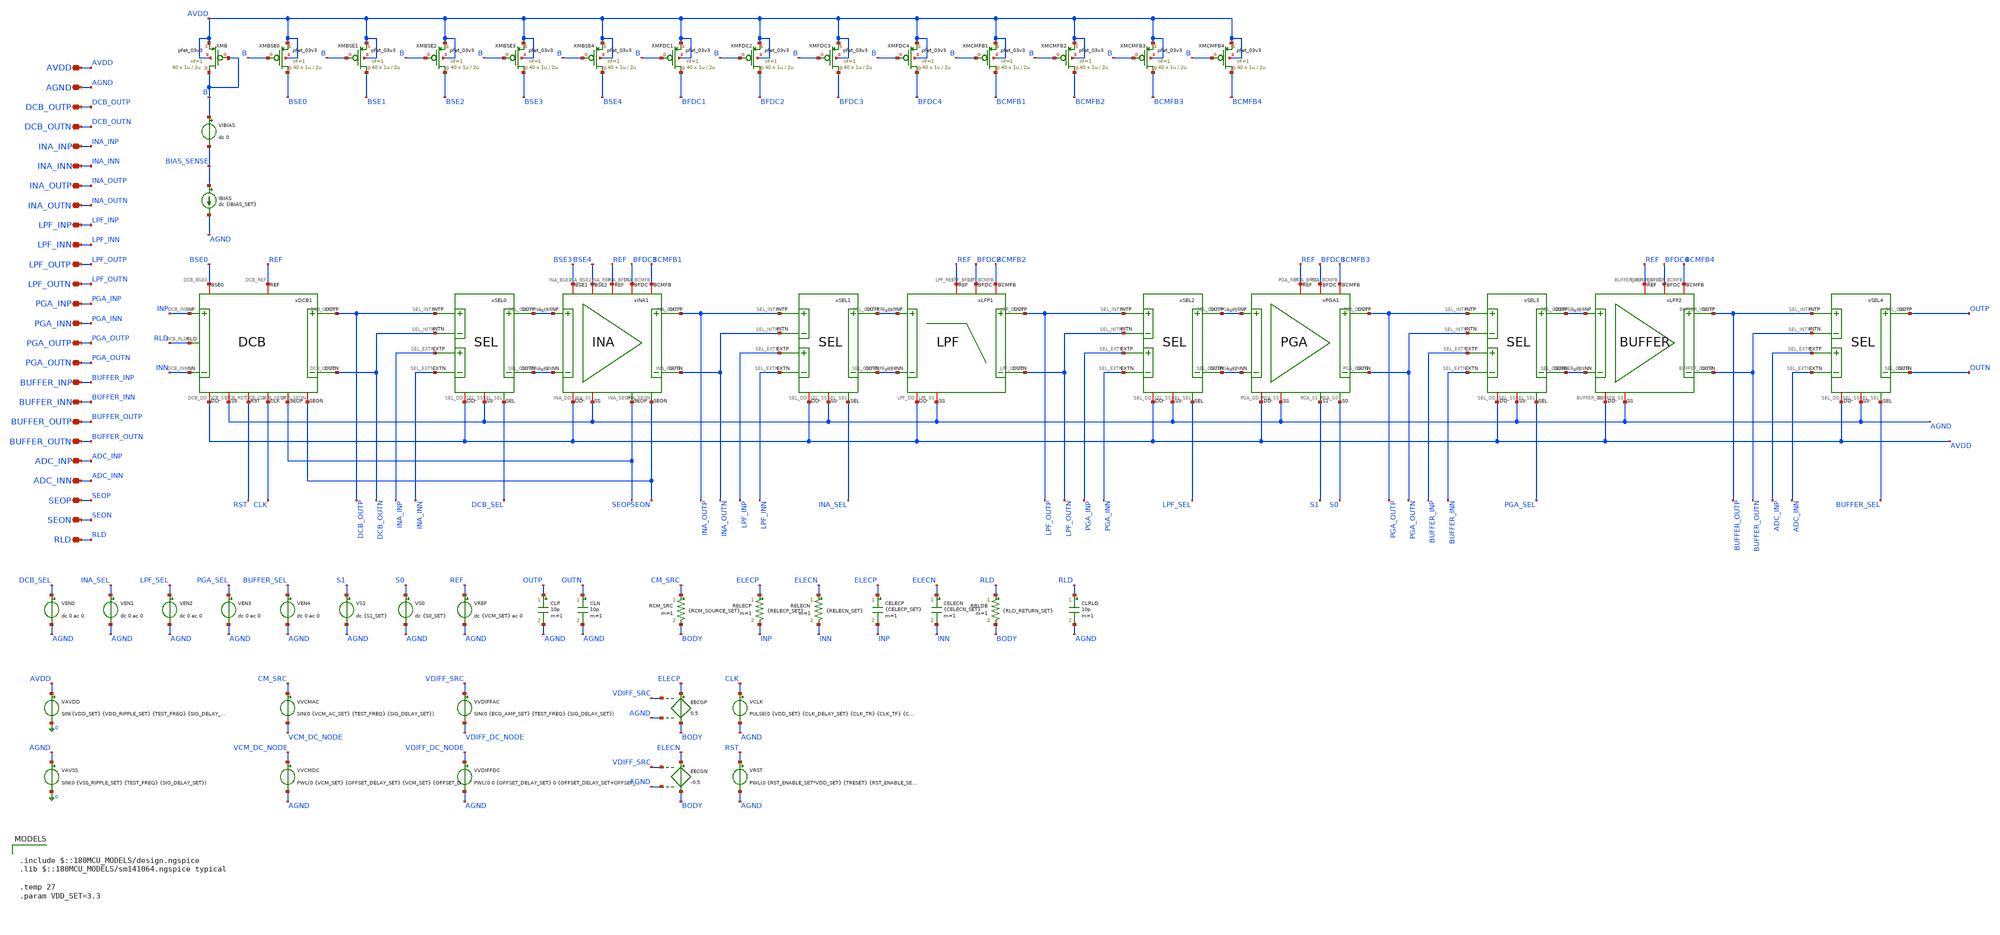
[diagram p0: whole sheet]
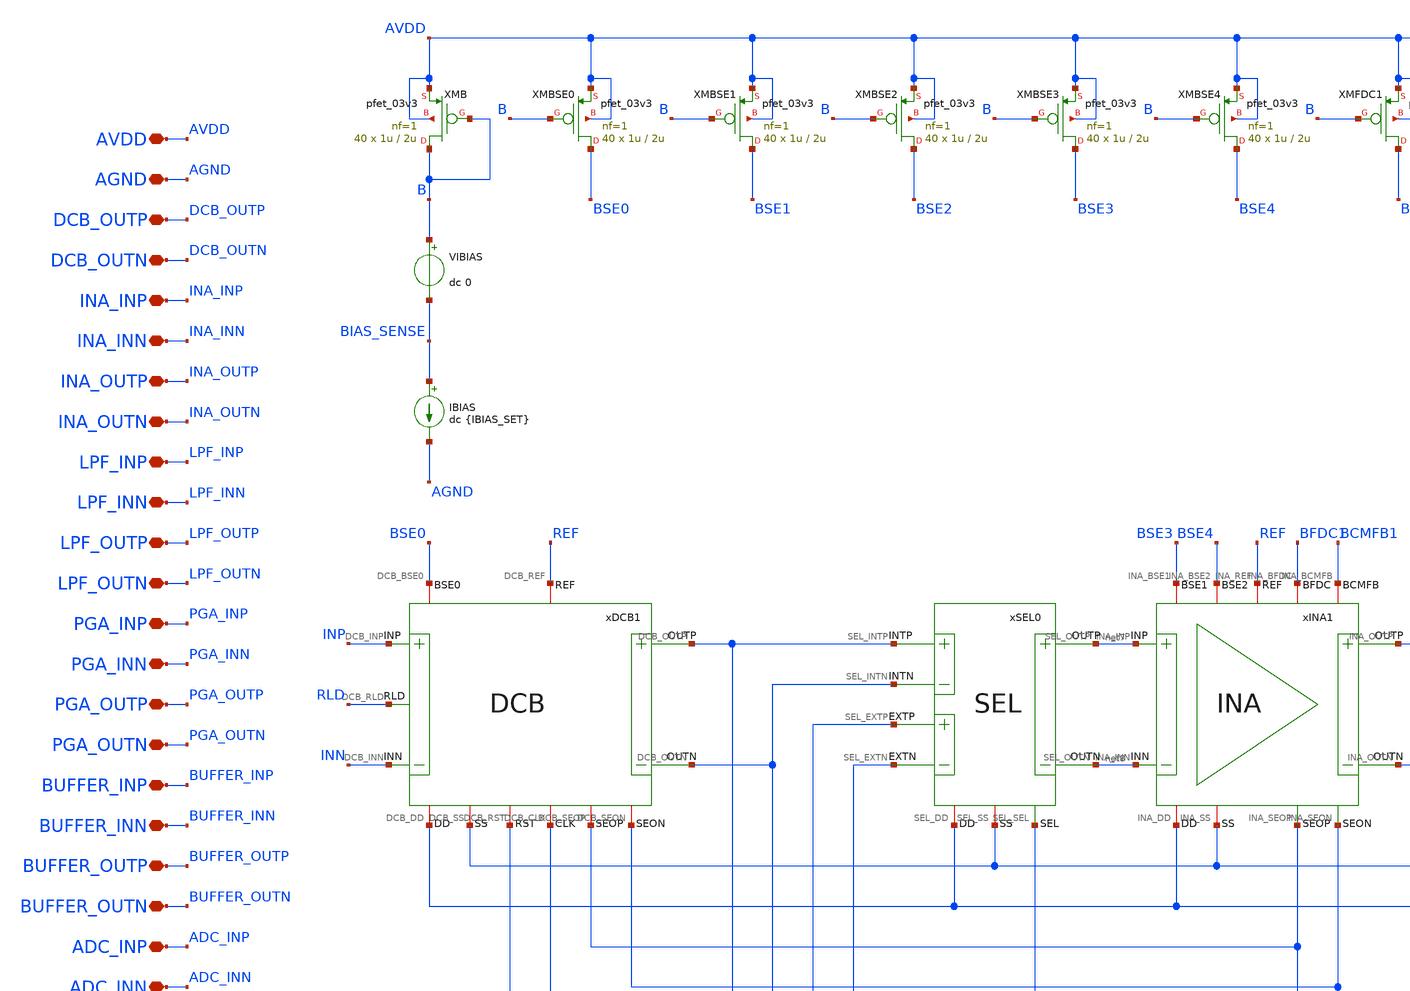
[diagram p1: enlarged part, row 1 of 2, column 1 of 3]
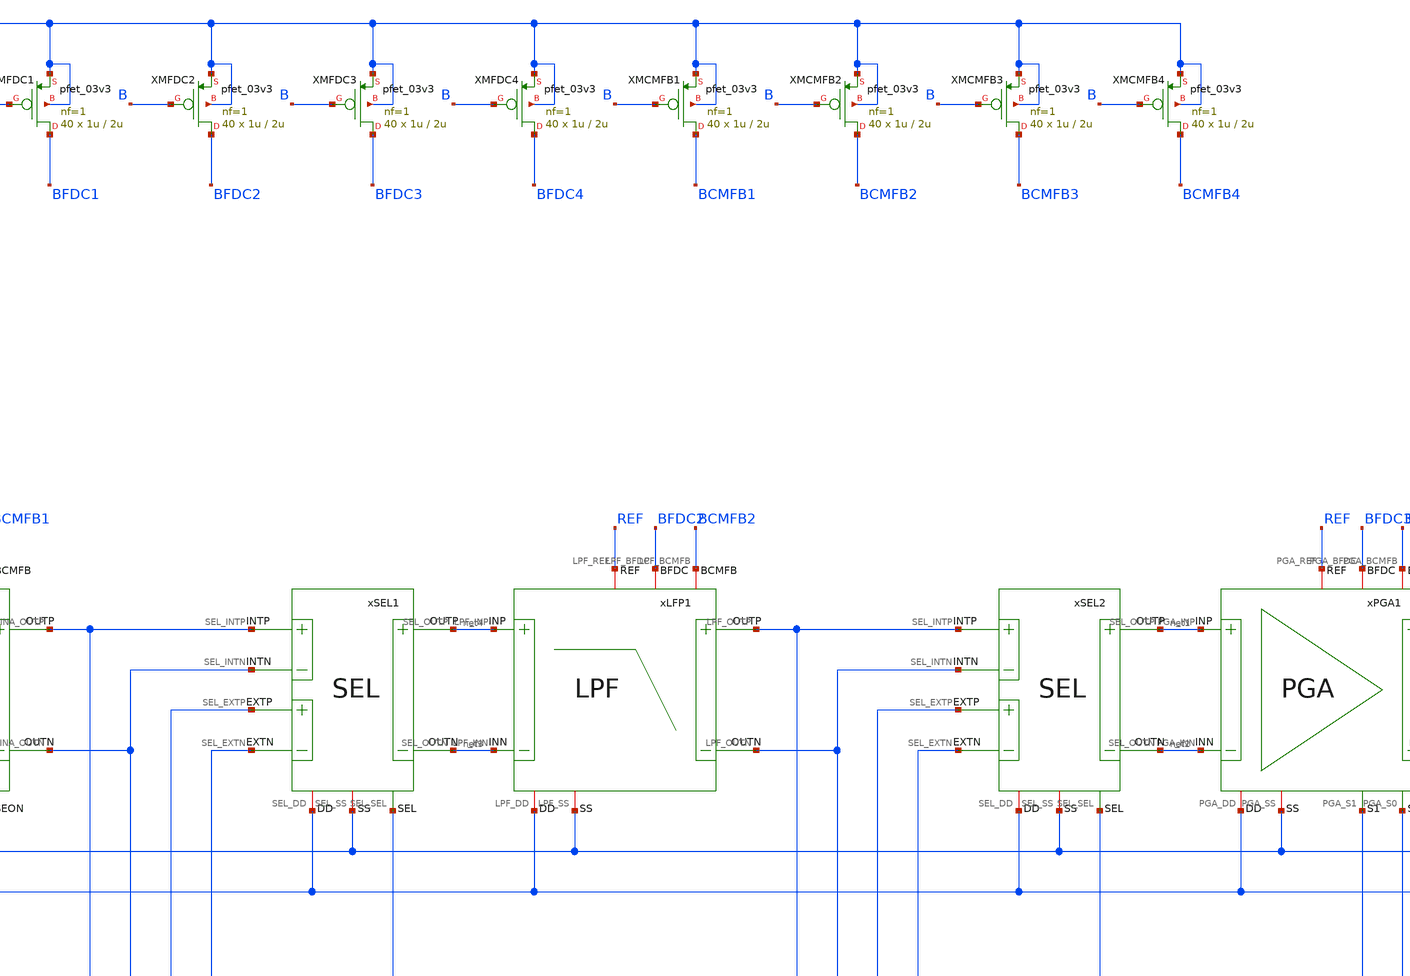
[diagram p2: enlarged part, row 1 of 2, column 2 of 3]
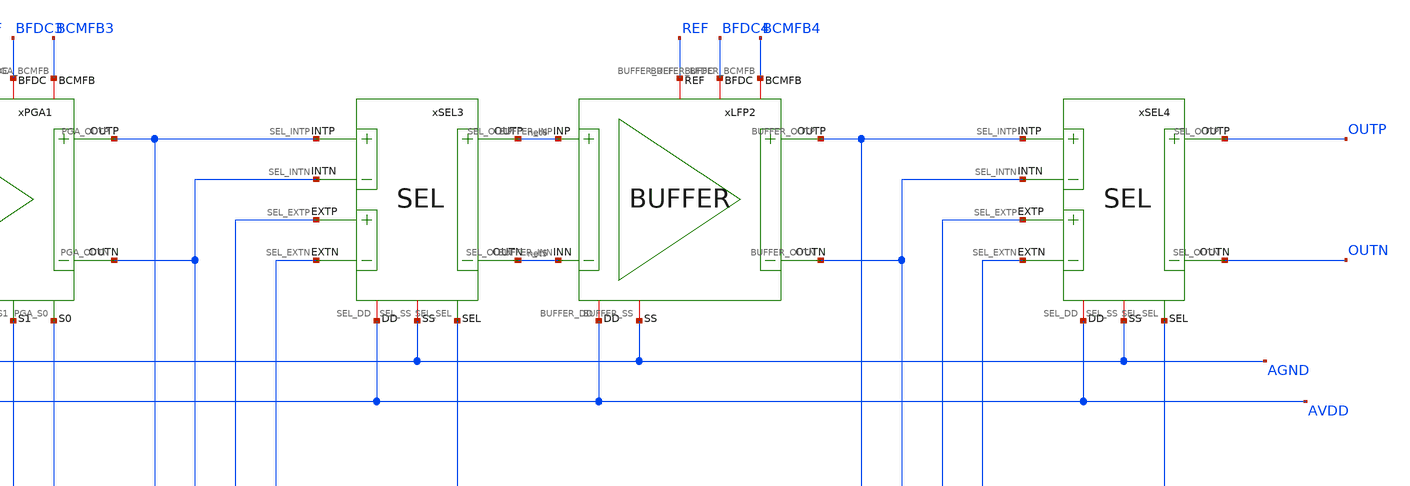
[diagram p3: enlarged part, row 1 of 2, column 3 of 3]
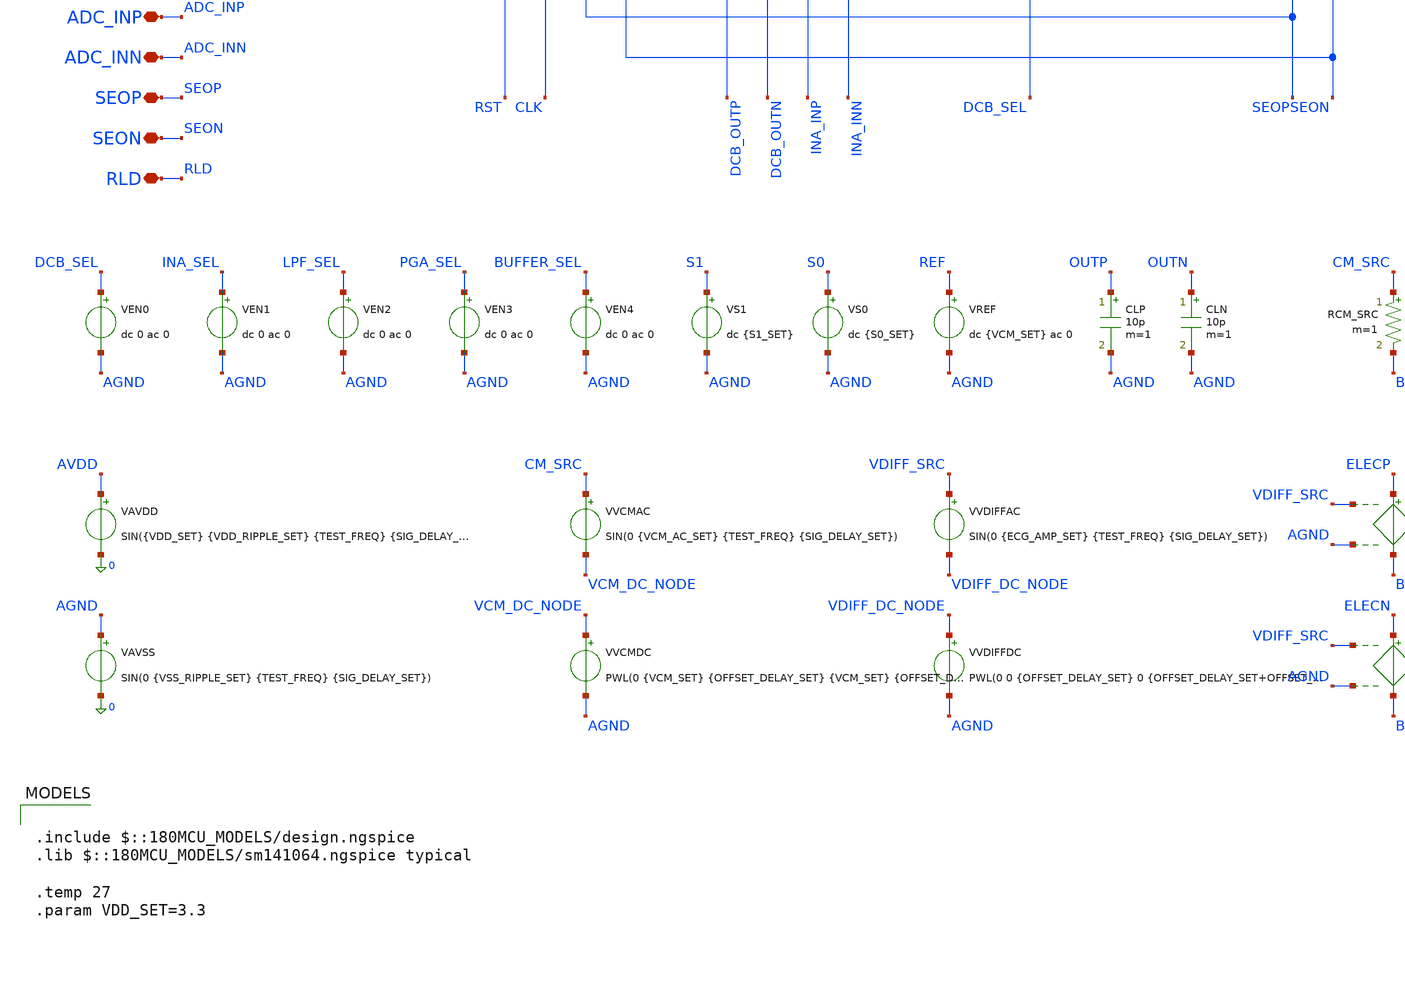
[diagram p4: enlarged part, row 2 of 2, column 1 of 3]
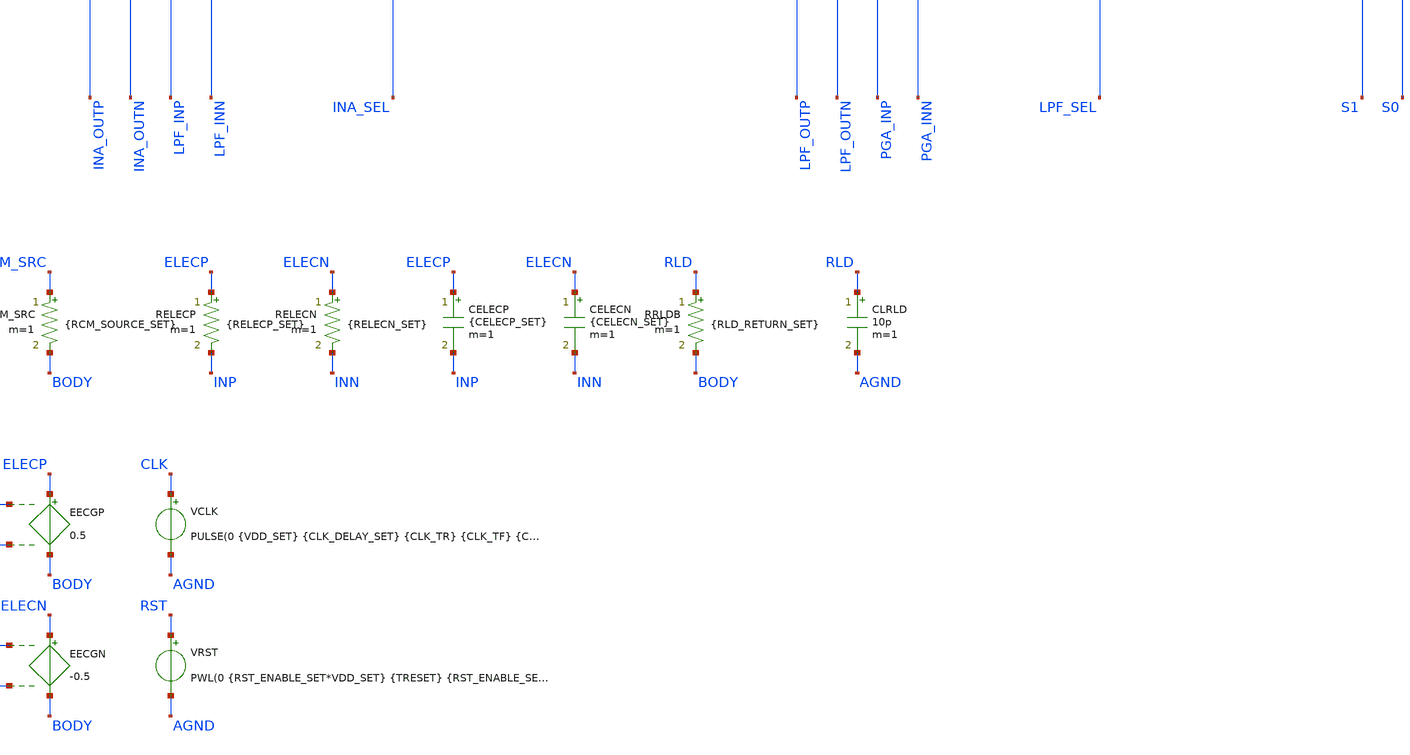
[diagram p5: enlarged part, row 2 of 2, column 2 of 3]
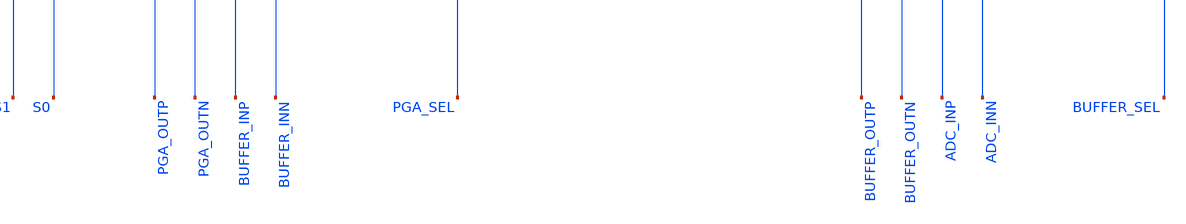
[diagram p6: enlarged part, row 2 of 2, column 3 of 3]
** sch_path: Design_Files/IC Design/Testbench/PATH/TRAN/PATH_TB_TRAN.sch
**.subckt PATH_TB_TRAN DCB_OUTP DCB_OUTN INA_INP INA_INN INA_OUTP INA_OUTN LPF_INP LPF_INN LPF_OUTP
*+ LPF_OUTN PGA_INP PGA_INN PGA_OUTP PGA_OUTN BUFFER_INP BUFFER_INN BUFFER_OUTP BUFFER_OUTN ADC_INP ADC_INN
*+ AVDD AGND SEOP SEON RLD
*.iopin DCB_OUTP
*.iopin DCB_OUTN
*.iopin INA_INP
*.iopin INA_INN
*.iopin INA_OUTP
*.iopin INA_OUTN
*.iopin LPF_INP
*.iopin LPF_INN
*.iopin LPF_OUTP
*.iopin LPF_OUTN
*.iopin PGA_INP
*.iopin PGA_INN
*.iopin PGA_OUTP
*.iopin PGA_OUTN
*.iopin BUFFER_INP
*.iopin BUFFER_INN
*.iopin BUFFER_OUTP
*.iopin BUFFER_OUTN
*.iopin ADC_INP
*.iopin ADC_INN
*.iopin AVDD
*.iopin AGND
*.iopin SEOP
*.iopin SEON
*.iopin RLD
VAVDD AVDD 0 SIN({VDD_SET} {VDD_RIPPLE_SET} {TEST_FREQ} {SIG_DELAY_SET})
.save i(vavdd)
VAVSS AGND 0 SIN(0 {VSS_RIPPLE_SET} {TEST_FREQ} {SIG_DELAY_SET})
.save i(vavss)
CLP OUTP AGND 10p m=1
CLN OUTN AGND 10p m=1
VIBIAS B BIAS_SENSE dc 0
.save i(vibias)
IBIAS BIAS_SENSE AGND dc {IBIAS_SET}
VREF REF AGND dc {VCM_SET} ac 0
xLFP1 AVDD AGND net4 net3 LPF_OUTN BFDC2 LPF_OUTP BCMFB2 REF LPF
xPGA1 AVDD AGND net1 net2 PGA_OUTN BFDC3 PGA_OUTP BCMFB3 REF S1 S0 PGA
xSEL1 AVDD AGND INA_OUTP INA_OUTN net3 net4 LPF_INP LPF_INN INA_SEL SEL
xINA1 AVDD AGND net7 net8 INA_OUTN BFDC1 INA_OUTP BCMFB1 REF SEON SEOP BSE3 BSE4 INA
xSEL2 AVDD AGND LPF_OUTP LPF_OUTN net2 net1 PGA_INP PGA_INN LPF_SEL SEL
xSEL3 AVDD AGND PGA_OUTP PGA_OUTN net5 net6 BUFFER_INP BUFFER_INN PGA_SEL SEL
xSEL4 AVDD AGND BUFFER_OUTP BUFFER_OUTN OUTN OUTP ADC_INP ADC_INN BUFFER_SEL SEL
xLFP2 AVDD AGND net6 net5 BUFFER_OUTN BFDC4 BUFFER_OUTP BCMFB4 REF BUFFER
VEN1 INA_SEL AGND dc 0 ac 0
.save i(ven1)
VS0 S0 AGND dc {S0_SET}
VS1 S1 AGND dc {S1_SET}
xSEL0 AVDD AGND DCB_OUTP DCB_OUTN net8 net7 INA_INP INA_INN DCB_SEL SEL
xDCB1 AVDD AGND INP INN DCB_OUTP DCB_OUTN RST CLK SEOP SEON REF BSE0 RLD DCB
VEN2 LPF_SEL AGND dc 0 ac 0
.save i(ven2)
VEN3 PGA_SEL AGND dc 0 ac 0
.save i(ven3)
VEN4 BUFFER_SEL AGND dc 0 ac 0
.save i(ven4)
VEN0 DCB_SEL AGND dc 0 ac 0
.save i(ven0)
VRST RST AGND PWL(0 {RST_ENABLE_SET*VDD_SET} {TRESET} {RST_ENABLE_SET*VDD_SET} {TRESET_END} 0 {RST_PULSE_ON_SET}
+ 0 {RST_PULSE_ON_END_SET} {RST_PULSE_ENABLE_SET*VDD_SET} {RST_PULSE_OFF_SET} {RST_PULSE_ENABLE_SET*VDD_SET}
+ {RST_PULSE_OFF_END_SET} 0)
VCLK CLK AGND PULSE(0 {VDD_SET} {CLK_DELAY_SET} {CLK_TR} {CLK_TF} {CLK_PW} {1/CLK_FREQ})
.save i(vclk)
CLRLD RLD AGND 10p m=1
RCM_SRC CM_SRC BODY {RCM_SOURCE_SET} m=1
RELECP ELECP INP {RELECP_SET} m=1
RELECN ELECN INN {RELECN_SET} m=1
CELECP ELECP INP {CELECP_SET} m=1
CELECN ELECN INN {CELECN_SET} m=1
RRLDB RLD BODY {RLD_RETURN_SET} m=1
VVCMAC CM_SRC VCM_DC_NODE SIN(0 {VCM_AC_SET} {TEST_FREQ} {SIG_DELAY_SET})
VVCMDC VCM_DC_NODE AGND PWL(0 {VCM_SET} {OFFSET_DELAY_SET} {VCM_SET} {OFFSET_DELAY_SET+OFFSET_RISE_SET}
+ {VCM_SET+VCM_DC_SET})
VVDIFFAC VDIFF_SRC VDIFF_DC_NODE SIN(0 {ECG_AMP_SET} {TEST_FREQ} {SIG_DELAY_SET})
VVDIFFDC VDIFF_DC_NODE AGND PWL(0 0 {OFFSET_DELAY_SET} 0 {OFFSET_DELAY_SET+OFFSET_RISE_SET} {VDIFF_DC_SET})
EECGP ELECP BODY VDIFF_SRC AGND 0.5
EECGN ELECN BODY VDIFF_SRC AGND -0.5
XMB B B AVDD AVDD pfet_03v3 L=2u W=1u nf=1 ad='int((nf+1)/2) * W/nf * 0.18u' as='int((nf+2)/2) * W/nf * 0.18u'
+ pd='2*int((nf+1)/2) * (W/nf + 0.18u)' ps='2*int((nf+2)/2) * (W/nf + 0.18u)' nrd='0.18u / W' nrs='0.18u / W'
+ sa=0 sb=0 sd=0 m=40
XMBSE3 BSE3 B AVDD AVDD pfet_03v3 L=2u W=1u nf=1 ad='int((nf+1)/2) * W/nf * 0.18u' as='int((nf+2)/2) * W/nf * 0.18u'
+ pd='2*int((nf+1)/2) * (W/nf + 0.18u)' ps='2*int((nf+2)/2) * (W/nf + 0.18u)' nrd='0.18u / W' nrs='0.18u / W'
+ sa=0 sb=0 sd=0 m=40
XMBSE4 BSE4 B AVDD AVDD pfet_03v3 L=2u W=1u nf=1 ad='int((nf+1)/2) * W/nf * 0.18u' as='int((nf+2)/2) * W/nf * 0.18u'
+ pd='2*int((nf+1)/2) * (W/nf + 0.18u)' ps='2*int((nf+2)/2) * (W/nf + 0.18u)' nrd='0.18u / W' nrs='0.18u / W'
+ sa=0 sb=0 sd=0 m=40
XMFDC1 BFDC1 B AVDD AVDD pfet_03v3 L=2u W=1u nf=1 ad='int((nf+1)/2) * W/nf * 0.18u' as='int((nf+2)/2) * W/nf * 0.18u'
+ pd='2*int((nf+1)/2) * (W/nf + 0.18u)' ps='2*int((nf+2)/2) * (W/nf + 0.18u)' nrd='0.18u / W' nrs='0.18u / W'
+ sa=0 sb=0 sd=0 m=40
XMFDC2 BFDC2 B AVDD AVDD pfet_03v3 L=2u W=1u nf=1 ad='int((nf+1)/2) * W/nf * 0.18u' as='int((nf+2)/2) * W/nf * 0.18u'
+ pd='2*int((nf+1)/2) * (W/nf + 0.18u)' ps='2*int((nf+2)/2) * (W/nf + 0.18u)' nrd='0.18u / W' nrs='0.18u / W'
+ sa=0 sb=0 sd=0 m=40
XMFDC3 BFDC3 B AVDD AVDD pfet_03v3 L=2u W=1u nf=1 ad='int((nf+1)/2) * W/nf * 0.18u' as='int((nf+2)/2) * W/nf * 0.18u'
+ pd='2*int((nf+1)/2) * (W/nf + 0.18u)' ps='2*int((nf+2)/2) * (W/nf + 0.18u)' nrd='0.18u / W' nrs='0.18u / W'
+ sa=0 sb=0 sd=0 m=40
XMFDC4 BFDC4 B AVDD AVDD pfet_03v3 L=2u W=1u nf=1 ad='int((nf+1)/2) * W/nf * 0.18u' as='int((nf+2)/2) * W/nf * 0.18u'
+ pd='2*int((nf+1)/2) * (W/nf + 0.18u)' ps='2*int((nf+2)/2) * (W/nf + 0.18u)' nrd='0.18u / W' nrs='0.18u / W'
+ sa=0 sb=0 sd=0 m=40
XMCMFB1 BCMFB1 B AVDD AVDD pfet_03v3 L=2u W=1u nf=1 ad='int((nf+1)/2) * W/nf * 0.18u' as='int((nf+2)/2) * W/nf * 0.18u'
+ pd='2*int((nf+1)/2) * (W/nf + 0.18u)' ps='2*int((nf+2)/2) * (W/nf + 0.18u)' nrd='0.18u / W' nrs='0.18u / W'
+ sa=0 sb=0 sd=0 m=40
XMCMFB2 BCMFB2 B AVDD AVDD pfet_03v3 L=2u W=1u nf=1 ad='int((nf+1)/2) * W/nf * 0.18u' as='int((nf+2)/2) * W/nf * 0.18u'
+ pd='2*int((nf+1)/2) * (W/nf + 0.18u)' ps='2*int((nf+2)/2) * (W/nf + 0.18u)' nrd='0.18u / W' nrs='0.18u / W'
+ sa=0 sb=0 sd=0 m=40
XMCMFB3 BCMFB3 B AVDD AVDD pfet_03v3 L=2u W=1u nf=1 ad='int((nf+1)/2) * W/nf * 0.18u' as='int((nf+2)/2) * W/nf * 0.18u'
+ pd='2*int((nf+1)/2) * (W/nf + 0.18u)' ps='2*int((nf+2)/2) * (W/nf + 0.18u)' nrd='0.18u / W' nrs='0.18u / W'
+ sa=0 sb=0 sd=0 m=40
XMCMFB4 BCMFB4 B AVDD AVDD pfet_03v3 L=2u W=1u nf=1 ad='int((nf+1)/2) * W/nf * 0.18u' as='int((nf+2)/2) * W/nf * 0.18u'
+ pd='2*int((nf+1)/2) * (W/nf + 0.18u)' ps='2*int((nf+2)/2) * (W/nf + 0.18u)' nrd='0.18u / W' nrs='0.18u / W'
+ sa=0 sb=0 sd=0 m=40
XMBSE1 BSE1 B AVDD AVDD pfet_03v3 L=2u W=1u nf=1 ad='int((nf+1)/2) * W/nf * 0.18u' as='int((nf+2)/2) * W/nf * 0.18u'
+ pd='2*int((nf+1)/2) * (W/nf + 0.18u)' ps='2*int((nf+2)/2) * (W/nf + 0.18u)' nrd='0.18u / W' nrs='0.18u / W'
+ sa=0 sb=0 sd=0 m=40
XMBSE2 BSE2 B AVDD AVDD pfet_03v3 L=2u W=1u nf=1 ad='int((nf+1)/2) * W/nf * 0.18u' as='int((nf+2)/2) * W/nf * 0.18u'
+ pd='2*int((nf+1)/2) * (W/nf + 0.18u)' ps='2*int((nf+2)/2) * (W/nf + 0.18u)' nrd='0.18u / W' nrs='0.18u / W'
+ sa=0 sb=0 sd=0 m=40
XMBSE0 BSE0 B AVDD AVDD pfet_03v3 L=2u W=1u nf=1 ad='int((nf+1)/2) * W/nf * 0.18u' as='int((nf+2)/2) * W/nf * 0.18u'
+ pd='2*int((nf+1)/2) * (W/nf + 0.18u)' ps='2*int((nf+2)/2) * (W/nf + 0.18u)' nrd='0.18u / W' nrs='0.18u / W'
+ sa=0 sb=0 sd=0 m=40
**** begin user architecture code

.include $::180MCU_MODELS/design.ngspice
.lib $::180MCU_MODELS/sm141064.ngspice typical

.temp 27
.param VDD_SET=3.3



.param VCM_SET={VDD_SET/2}
.param IBIAS_SET=40u

.param CLK_FREQ=500
.param CLK_TR=80u
.param CLK_TF=80u
.param CLK_PW={0.5/CLK_FREQ-CLK_TR}
.param CLK_DELAY_SET=1m

.param RST_ENABLE_SET=1
.param TRESET=10m
.param TRESET_END=10.001m

.param RST_PULSE_ENABLE_SET=0
.param RST_PULSE_ON_SET=40m
.param RST_PULSE_ON_END_SET=40.001m
.param RST_PULSE_OFF_SET=60m
.param RST_PULSE_OFF_END_SET=60.001m

.param SIG_DELAY_SET=100m

.param TEST_FREQ=60
.param ECG_AMP_SET=0

.param VDIFF_DC_SET=0
.param VCM_DC_SET=0
.param VCM_AC_SET=0

.param OFFSET_DELAY_SET=20m
.param OFFSET_RISE_SET=10m

.param VDD_RIPPLE_SET=0
.param VSS_RIPPLE_SET=0

.param S1_SET=3.3
.param S0_SET=3.3

.param RCM_SOURCE_SET=1

.param RELECP_SET=1
.param RELECN_SET=1

.param CELECP_SET=1f
.param CELECN_SET=1f

.param RLD_RETURN_SET=100T

.options method=gear
.options maxord=2

.options reltol=5e-3
.options abstol=1e-11
.options vntol=20u
.options chgtol=5e-13

.options itl1=1000
.options itl2=500
.options itl4=1500

.options gmin=1e-11
.options gminsteps=20
.options srcsteps=20
.options rshunt=100T

.options plotwinsize=0

.nodeset v(B)=2.3
.nodeset v(BODY)={VCM_SET}

.nodeset v(INP)={VCM_SET}
.nodeset v(INN)={VCM_SET}

.nodeset v(OUTP)={VCM_SET}
.nodeset v(OUTN)={VCM_SET}

.nodeset v(RLD)={VCM_SET}

.save v(AVDD) v(AGND)
.save v(BODY)
.save v(INP) v(INN)
.save v(OUTP) v(OUTN)
.save v(RLD)
.save v(RST) v(CLK)





.control

destroy all

set noaskquit
set wr_singlescale
unset wr_vecnames
set appendwrite

option numdgt=15
option sparse
option method=gear
option maxord=2
option plotwinsize=0

shell mkdir -p
+ /foss/designs/ECG_Acquisition_IC/Measurement_Results/IC_Simulation/PATH/NOM.Result_txt

shell rm -f
+ /foss/designs/ECG_Acquisition_IC/Measurement_Results/IC_Simulation/PATH/NOM.Result_txt/NOM.diff_tran.txt
shell rm -f
+ /foss/designs/ECG_Acquisition_IC/Measurement_Results/IC_Simulation/PATH/NOM.Result_txt/NOM.cmrr_tran.txt
shell rm -f
+ /foss/designs/ECG_Acquisition_IC/Measurement_Results/IC_Simulation/PATH/NOM.Result_txt/NOM.psrrp_tran.txt
shell rm -f
+ /foss/designs/ECG_Acquisition_IC/Measurement_Results/IC_Simulation/PATH/NOM.Result_txt/NOM.psrrn_tran.txt

shell rm -f
+ /foss/designs/ECG_Acquisition_IC/Measurement_Results/IC_Simulation/PATH/NOM.Result_txt/NOM.vcmdcoffset_tran.txt
shell rm -f
+ /foss/designs/ECG_Acquisition_IC/Measurement_Results/IC_Simulation/PATH/NOM.Result_txt/NOM.vdiffdcoffset_tran.txt

shell rm -f
+ /foss/designs/ECG_Acquisition_IC/Measurement_Results/IC_Simulation/PATH/NOM.Result_txt/NOM.startup_with_reset.txt
shell rm -f
+ /foss/designs/ECG_Acquisition_IC/Measurement_Results/IC_Simulation/PATH/NOM.Result_txt/NOM.startup_without_reset.txt

shell rm -f
+ /foss/designs/ECG_Acquisition_IC/Measurement_Results/IC_Simulation/PATH/NOM.Result_txt/NOM.rld_off.txt
shell rm -f
+ /foss/designs/ECG_Acquisition_IC/Measurement_Results/IC_Simulation/PATH/NOM.Result_txt/NOM.rld_on.txt

shell rm -f
+ /foss/designs/ECG_Acquisition_IC/Measurement_Results/IC_Simulation/PATH/NOM.Result_txt/NOM.thd_tran.txt


* Common
alterparam CLK_FREQ=500
alterparam CLK_TR=80u
alterparam CLK_TF=80u
alterparam CLK_PW=920u
alterparam CLK_DELAY_SET=1m

alterparam ECG_AMP_SET=0
alterparam VDIFF_DC_SET=0

alterparam VCM_DC_SET=0
alterparam VCM_AC_SET=0

alterparam VDD_RIPPLE_SET=0
alterparam VSS_RIPPLE_SET=0

alterparam RST_ENABLE_SET=1
alterparam TRESET=10m
alterparam TRESET_END=10.001m

alterparam RST_PULSE_ENABLE_SET=0
alterparam RST_PULSE_ON_SET=40m
alterparam RST_PULSE_ON_END_SET=40.001m
alterparam RST_PULSE_OFF_SET=60m
alterparam RST_PULSE_OFF_END_SET=60.001m

alterparam SIG_DELAY_SET=100m

alterparam OFFSET_DELAY_SET=20m
alterparam OFFSET_RISE_SET=10m

alterparam RCM_SOURCE_SET=1

alterparam RELECP_SET=1
alterparam RELECN_SET=1

alterparam CELECP_SET=1f
alterparam CELECN_SET=1f

alterparam RLD_RETURN_SET=100T

alterparam S1_SET=3.3
alterparam S0_SET=3.3


* Differential response
alterparam ECG_AMP_SET=10u
alterparam VDIFF_DC_SET=0

alterparam VCM_DC_SET=0
alterparam VCM_AC_SET=0

alterparam VDD_RIPPLE_SET=0
alterparam VSS_RIPPLE_SET=0

alterparam RST_ENABLE_SET=0
alterparam RST_PULSE_ENABLE_SET=1

foreach gaincfg 0 1

    if $gaincfg = 0
        alterparam S1_SET=0
        alterparam S0_SET=0
    else
        alterparam S1_SET=3.3
        alterparam S0_SET=3.3
    end

    foreach freq 150 60 0.05

        alterparam TEST_FREQ=$freq
        reset

        option method=gear
        option maxord=2
        option plotwinsize=0

        setplot const

        let ncycle=11
        let tprint=100u
        let tmax=20u

        if $freq > 500
            let tprint=50u
        end

        if $freq < 1
            let ncycle=2
            let tprint=500u
        end

        let tstop=0.100+ncycle/$freq

        tran $&tprint $&tstop 0 $&tmax

        let tr_freq=time*0+$freq

        if $gaincfg = 0
            let tr_pga_gain=time*0+2
        else
            let tr_pga_gain=time*0+16
        end

        let tr_vin_cm=0.5*(v(INP)+v(INN))-v(AGND)
        let tr_vin_diff=v(INP)-v(INN)

        let tr_vout_cm=0.5*(v(OUTP)+v(OUTN))-v(AGND)
        let tr_vout_diff=v(OUTP)-v(OUTN)

        setscale time

        wrdata
+ /foss/designs/ECG_Acquisition_IC/Measurement_Results/IC_Simulation/PATH/NOM.Result_txt/NOM.diff_tran.txt tr_pga_gain tr_freq tr_vin_cm tr_vin_diff tr_vout_cm tr_vout_diff v(RST)

        destroy $curplot

    end
end


* CMRR
alterparam ECG_AMP_SET=0
alterparam VDIFF_DC_SET=0

alterparam VCM_DC_SET=0
alterparam VCM_AC_SET=10m

alterparam VDD_RIPPLE_SET=0
alterparam VSS_RIPPLE_SET=0

alterparam RST_ENABLE_SET=0
alterparam RST_PULSE_ENABLE_SET=1

foreach gaincfg 0 1

    if $gaincfg = 0
        alterparam S1_SET=0
        alterparam S0_SET=0
    else
        alterparam S1_SET=3.3
        alterparam S0_SET=3.3
    end

    foreach freq 1000 150 60 0.05

        alterparam TEST_FREQ=$freq
        reset

        option method=gear
        option maxord=2
        option plotwinsize=0

        setplot const

        let ncycle=11
        let tprint=100u
        let tmax=20u

        if $freq > 500
            let tprint=50u
        end

        if $freq < 1
            let ncycle=2
            let tprint=500u
        end

        let tstop=0.100+ncycle/$freq

        tran $&tprint $&tstop 0 $&tmax

        let tr_freq=time*0+$freq

        if $gaincfg = 0
            let tr_pga_gain=time*0+2
        else
            let tr_pga_gain=time*0+16
        end

        let tr_vin_cm=0.5*(v(INP)+v(INN))-v(AGND)

        let tr_vout_cm=0.5*(v(OUTP)+v(OUTN))-v(AGND)
        let tr_vout_diff=v(OUTP)-v(OUTN)

        setscale time

        wrdata
+ /foss/designs/ECG_Acquisition_IC/Measurement_Results/IC_Simulation/PATH/NOM.Result_txt/NOM.cmrr_tran.txt tr_pga_gain tr_freq tr_vin_cm tr_vout_cm tr_vout_diff v(RST)

        destroy $curplot

    end
end


* PSRR+
alterparam ECG_AMP_SET=0
alterparam VDIFF_DC_SET=0

alterparam VCM_DC_SET=0
alterparam VCM_AC_SET=0

alterparam VDD_RIPPLE_SET=10m
alterparam VSS_RIPPLE_SET=0

alterparam RST_ENABLE_SET=0
alterparam RST_PULSE_ENABLE_SET=1

foreach gaincfg 0 1

    if $gaincfg = 0
        alterparam S1_SET=0
        alterparam S0_SET=0
    else
        alterparam S1_SET=3.3
        alterparam S0_SET=3.3
    end

    foreach freq 1000 150 60 0.05

        alterparam TEST_FREQ=$freq
        reset

        option method=gear
        option maxord=2
        option plotwinsize=0

        setplot const

        let ncycle=11
        let tprint=100u
        let tmax=20u

        if $freq > 500
            let tprint=50u
        end

        if $freq < 1
            let ncycle=2
            let tprint=500u
        end

        let tstop=0.100+ncycle/$freq

        tran $&tprint $&tstop 0 $&tmax

        let tr_freq=time*0+$freq

        if $gaincfg = 0
            let tr_pga_gain=time*0+2
        else
            let tr_pga_gain=time*0+16
        end

        let tr_supply_in=v(AVDD)-v(AGND)

        let tr_vout_cm=0.5*(v(OUTP)+v(OUTN))-v(AGND)
        let tr_vout_diff=v(OUTP)-v(OUTN)

        setscale time

        wrdata
+ /foss/designs/ECG_Acquisition_IC/Measurement_Results/IC_Simulation/PATH/NOM.Result_txt/NOM.psrrp_tran.txt tr_pga_gain tr_freq tr_supply_in tr_vout_cm tr_vout_diff v(RST)

        destroy $curplot

    end
end


* PSRR-
alterparam ECG_AMP_SET=0
alterparam VDIFF_DC_SET=0

alterparam VCM_DC_SET=0
alterparam VCM_AC_SET=0

alterparam VDD_RIPPLE_SET=0
alterparam VSS_RIPPLE_SET=10m

alterparam RST_ENABLE_SET=0
alterparam RST_PULSE_ENABLE_SET=1

foreach gaincfg 0 1

    if $gaincfg = 0
        alterparam S1_SET=0
        alterparam S0_SET=0
    else
        alterparam S1_SET=3.3
        alterparam S0_SET=3.3
    end

    foreach freq 1000 150 60 0.05

        alterparam TEST_FREQ=$freq
        reset

        option method=gear
        option maxord=2
        option plotwinsize=0

        setplot const

        let ncycle=11
        let tprint=100u
        let tmax=20u

        if $freq > 500
            let tprint=50u
        end

        if $freq < 1
            let ncycle=2
            let tprint=500u
        end

        let tstop=0.100+ncycle/$freq

        tran $&tprint $&tstop 0 $&tmax

        let tr_freq=time*0+$freq

        if $gaincfg = 0
            let tr_pga_gain=time*0+2
        else
            let tr_pga_gain=time*0+16
        end

        let tr_supply_in=v(AGND)

        let tr_vout_cm=0.5*(v(OUTP)+v(OUTN))-v(AGND)
        let tr_vout_diff=v(OUTP)-v(OUTN)

        setscale time

        wrdata
+ /foss/designs/ECG_Acquisition_IC/Measurement_Results/IC_Simulation/PATH/NOM.Result_txt/NOM.psrrn_tran.txt tr_pga_gain tr_freq tr_supply_in tr_vout_cm tr_vout_diff v(RST)

        destroy $curplot

    end
end

alterparam VDD_RIPPLE_SET=0
alterparam VSS_RIPPLE_SET=0


* VCM offset
alterparam TEST_FREQ=60

alterparam ECG_AMP_SET=0
alterparam VDIFF_DC_SET=0

alterparam VCM_DC_SET=0
alterparam VCM_AC_SET=0

alterparam VDD_RIPPLE_SET=0
alterparam VSS_RIPPLE_SET=0

alterparam RST_ENABLE_SET=0
alterparam RST_PULSE_ENABLE_SET=1

foreach cfg 0 1

    if $cfg = 0
        alterparam ECG_AMP_SET=0.25m
        alterparam S1_SET=3.3
        alterparam S0_SET=3.3
    else
        alterparam ECG_AMP_SET=2.5m
        alterparam S1_SET=0
        alterparam S0_SET=0
    end

    foreach off 500m 300m 0 -300m -500m

        alterparam VCM_DC_SET=$off
        reset

        option method=gear
        option maxord=2
        option plotwinsize=0

        tran 100u 300m 0 20u

        let tr_cfg=time*0+$cfg
        let tr_offset=time*0+$off

        if $cfg = 0
            let tr_input_pp=time*0+0.5m
            let tr_pga_gain=time*0+16
        else
            let tr_input_pp=time*0+5m
            let tr_pga_gain=time*0+2
        end

        let tr_vin_cm=0.5*(v(INP)+v(INN))-v(AGND)
        let tr_vin_diff=v(INP)-v(INN)

        let tr_vout_cm=0.5*(v(OUTP)+v(OUTN))-v(AGND)
        let tr_vout_diff=v(OUTP)-v(OUTN)

        let tr_rld=v(RLD)-v(AGND)

        setscale time

        wrdata
+ /foss/designs/ECG_Acquisition_IC/Measurement_Results/IC_Simulation/PATH/NOM.Result_txt/NOM.vcmdcoffset_tran.txt tr_cfg tr_input_pp tr_pga_gain tr_offset v(RST) v(CLK) tr_vin_cm tr_vin_diff tr_vout_cm
+ tr_vout_diff tr_rld

        destroy $curplot

    end
end

alterparam VCM_DC_SET=0


* Differential offset
alterparam TEST_FREQ=60

alterparam VCM_DC_SET=0
alterparam VCM_AC_SET=0

alterparam VDD_RIPPLE_SET=0
alterparam VSS_RIPPLE_SET=0

alterparam RST_ENABLE_SET=0
alterparam RST_PULSE_ENABLE_SET=1

foreach cfg 0 1

    if $cfg = 0
        alterparam ECG_AMP_SET=0.25m
        alterparam S1_SET=3.3
        alterparam S0_SET=3.3
    else
        alterparam ECG_AMP_SET=2.5m
        alterparam S1_SET=0
        alterparam S0_SET=0
    end

    foreach off 500m 300m 0 -300m -500m

        alterparam VDIFF_DC_SET=$off
        reset

        option method=gear
        option maxord=2
        option plotwinsize=0

        tran 100u 300m 0 20u

        let tr_cfg=time*0+$cfg
        let tr_offset=time*0+$off

        if $cfg = 0
            let tr_input_pp=time*0+0.5m
            let tr_pga_gain=time*0+16
        else
            let tr_input_pp=time*0+5m
            let tr_pga_gain=time*0+2
        end

        let tr_vin_cm=0.5*(v(INP)+v(INN))-v(AGND)
        let tr_vin_diff=v(INP)-v(INN)

        let tr_vout_cm=0.5*(v(OUTP)+v(OUTN))-v(AGND)
        let tr_vout_diff=v(OUTP)-v(OUTN)

        let tr_rld=v(RLD)-v(AGND)

        setscale time

        wrdata
+ /foss/designs/ECG_Acquisition_IC/Measurement_Results/IC_Simulation/PATH/NOM.Result_txt/NOM.vdiffdcoffset_tran.txt tr_cfg tr_input_pp tr_pga_gain tr_offset v(RST) v(CLK) tr_vin_cm tr_vin_diff tr_vout_cm
+ tr_vout_diff tr_rld

        destroy $curplot

    end
end

alterparam VDIFF_DC_SET=0


* Startup with reset
alterparam TEST_FREQ=60
alterparam ECG_AMP_SET=0

alterparam VDIFF_DC_SET=300m
alterparam VCM_DC_SET=0
alterparam VCM_AC_SET=0

alterparam VDD_RIPPLE_SET=0
alterparam VSS_RIPPLE_SET=0

alterparam S1_SET=3.3
alterparam S0_SET=3.3

alterparam RST_ENABLE_SET=0
alterparam RST_PULSE_ENABLE_SET=1

reset

option method=gear
option maxord=2
option plotwinsize=0

tran 100u 200m 0 20u

let tr_vin_cm=0.5*(v(INP)+v(INN))-v(AGND)
let tr_vin_diff=v(INP)-v(INN)

let tr_vout_cm=0.5*(v(OUTP)+v(OUTN))-v(AGND)
let tr_vout_diff=v(OUTP)-v(OUTN)

let tr_outp=v(OUTP)-v(AGND)
let tr_outn=v(OUTN)-v(AGND)

let tr_rld=v(RLD)-v(AGND)

setscale time

wrdata
+ /foss/designs/ECG_Acquisition_IC/Measurement_Results/IC_Simulation/PATH/NOM.Result_txt/NOM.startup_with_reset.txt v(RST) v(CLK) tr_vin_cm tr_vin_diff tr_vout_cm tr_vout_diff tr_outp tr_outn tr_rld

destroy $curplot


* Startup without reset
alterparam RST_ENABLE_SET=0
alterparam RST_PULSE_ENABLE_SET=0

reset

option method=gear
option maxord=2
option plotwinsize=0

tran 100u 200m 0 20u

let tr_vin_cm=0.5*(v(INP)+v(INN))-v(AGND)
let tr_vin_diff=v(INP)-v(INN)

let tr_vout_cm=0.5*(v(OUTP)+v(OUTN))-v(AGND)
let tr_vout_diff=v(OUTP)-v(OUTN)

let tr_outp=v(OUTP)-v(AGND)
let tr_outn=v(OUTN)-v(AGND)

let tr_rld=v(RLD)-v(AGND)

setscale time

wrdata
+ /foss/designs/ECG_Acquisition_IC/Measurement_Results/IC_Simulation/PATH/NOM.Result_txt/NOM.startup_without_reset.txt v(RST) v(CLK) tr_vin_cm tr_vin_diff tr_vout_cm tr_vout_diff tr_outp tr_outn tr_rld

destroy $curplot

alterparam VDIFF_DC_SET=0


* RLD
alterparam TEST_FREQ=60

alterparam ECG_AMP_SET=0
alterparam VDIFF_DC_SET=0

alterparam VCM_DC_SET=0
alterparam VCM_AC_SET=100m

alterparam VDD_RIPPLE_SET=0
alterparam VSS_RIPPLE_SET=0

alterparam S1_SET=3.3
alterparam S0_SET=3.3

alterparam RCM_SOURCE_SET=1Meg

alterparam RELECP_SET=80k
alterparam RELECN_SET=120k

alterparam CELECP_SET=120n
alterparam CELECN_SET=80n

alterparam RST_ENABLE_SET=0
alterparam RST_PULSE_ENABLE_SET=1


* RLD off
alterparam RLD_RETURN_SET=100T
reset

option method=gear
option maxord=2
option plotwinsize=0

tran 100u 300m 0 20u

let tr_body=v(BODY)-v(AGND)

let tr_vin_cm=0.5*(v(INP)+v(INN))-v(AGND)
let tr_vin_diff=v(INP)-v(INN)

let tr_rld=v(RLD)-v(AGND)
let tr_irld=(v(RLD)-v(BODY))/100T

let tr_vout_cm=0.5*(v(OUTP)+v(OUTN))-v(AGND)
let tr_vout_diff=v(OUTP)-v(OUTN)

setscale time

wrdata
+ /foss/designs/ECG_Acquisition_IC/Measurement_Results/IC_Simulation/PATH/NOM.Result_txt/NOM.rld_off.txt tr_body tr_vin_cm tr_vin_diff tr_rld tr_irld tr_vout_cm tr_vout_diff v(RST)

destroy $curplot


* RLD on
alterparam RLD_RETURN_SET=1Meg
reset

option method=gear
option maxord=2
option plotwinsize=0

tran 100u 300m 0 20u

let tr_body=v(BODY)-v(AGND)

let tr_vin_cm=0.5*(v(INP)+v(INN))-v(AGND)
let tr_vin_diff=v(INP)-v(INN)

let tr_rld=v(RLD)-v(AGND)
let tr_irld=(v(RLD)-v(BODY))/1Meg

let tr_vout_cm=0.5*(v(OUTP)+v(OUTN))-v(AGND)
let tr_vout_diff=v(OUTP)-v(OUTN)

setscale time

wrdata
+ /foss/designs/ECG_Acquisition_IC/Measurement_Results/IC_Simulation/PATH/NOM.Result_txt/NOM.rld_on.txt tr_body tr_vin_cm tr_vin_diff tr_rld tr_irld tr_vout_cm tr_vout_diff v(RST)

destroy $curplot


* Restore RLD
alterparam RCM_SOURCE_SET=1

alterparam RELECP_SET=1
alterparam RELECN_SET=1

alterparam CELECP_SET=1f
alterparam CELECN_SET=1f

alterparam RLD_RETURN_SET=100T

alterparam VCM_AC_SET=0


* THD
alterparam CLK_TR=20u
alterparam CLK_TF=20u
alterparam CLK_PW=980u

alterparam VCM_DC_SET=0
alterparam VCM_AC_SET=0
alterparam VDIFF_DC_SET=0

alterparam VDD_RIPPLE_SET=0
alterparam VSS_RIPPLE_SET=0

alterparam RLD_RETURN_SET=100T

alterparam RST_ENABLE_SET=0
alterparam RST_PULSE_ENABLE_SET=1

foreach freq 60 150

    alterparam TEST_FREQ=$freq

    foreach cfg 0 1

        if $cfg = 0
            alterparam ECG_AMP_SET=0.25m
            alterparam S1_SET=3.3
            alterparam S0_SET=3.3
        else
            alterparam ECG_AMP_SET=2.5m
            alterparam S1_SET=0
            alterparam S0_SET=0
        end

        reset

        option method=trap
        option maxord=2
        option plotwinsize=0

        setplot const

        let tstop=0.100+11/$freq

        tran 20u $&tstop 0 5u

        let tr_cfg=time*0+$cfg
        let tr_freq=time*0+$freq

        if $cfg = 0
            let tr_vin_pp=time*0+0.5m
            let tr_pga_gain=time*0+16
        else
            let tr_vin_pp=time*0+5m
            let tr_pga_gain=time*0+2
        end

        let tr_vin_diff=v(INP)-v(INN)

        let tr_vout_cm=0.5*(v(OUTP)+v(OUTN))-v(AGND)
        let tr_vout_diff=v(OUTP)-v(OUTN)

        setscale time

        wrdata
+ /foss/designs/ECG_Acquisition_IC/Measurement_Results/IC_Simulation/PATH/NOM.Result_txt/NOM.thd_tran.txt tr_cfg tr_freq tr_vin_pp tr_pga_gain tr_vin_diff tr_vout_cm tr_vout_diff v(RST)

        destroy $curplot

    end
end


* Restore
alterparam CLK_FREQ=500
alterparam CLK_TR=80u
alterparam CLK_TF=80u
alterparam CLK_PW=920u
alterparam CLK_DELAY_SET=1m

alterparam ECG_AMP_SET=0

alterparam VDIFF_DC_SET=0
alterparam VCM_DC_SET=0
alterparam VCM_AC_SET=0

alterparam VDD_RIPPLE_SET=0
alterparam VSS_RIPPLE_SET=0

alterparam RST_ENABLE_SET=1
alterparam TRESET=10m
alterparam TRESET_END=10.001m

alterparam RST_PULSE_ENABLE_SET=0
alterparam RST_PULSE_ON_SET=40m
alterparam RST_PULSE_ON_END_SET=40.001m
alterparam RST_PULSE_OFF_SET=60m
alterparam RST_PULSE_OFF_END_SET=60.001m

alterparam SIG_DELAY_SET=100m

alterparam OFFSET_DELAY_SET=20m
alterparam OFFSET_RISE_SET=10m

alterparam RCM_SOURCE_SET=1

alterparam RELECP_SET=1
alterparam RELECN_SET=1

alterparam CELECP_SET=1f
alterparam CELECN_SET=1f

alterparam RLD_RETURN_SET=100T

alterparam S1_SET=3.3
alterparam S0_SET=3.3

option method=gear
option maxord=2
option plotwinsize=0

* quit
.endc


**** end user architecture code
**.ends
.end
